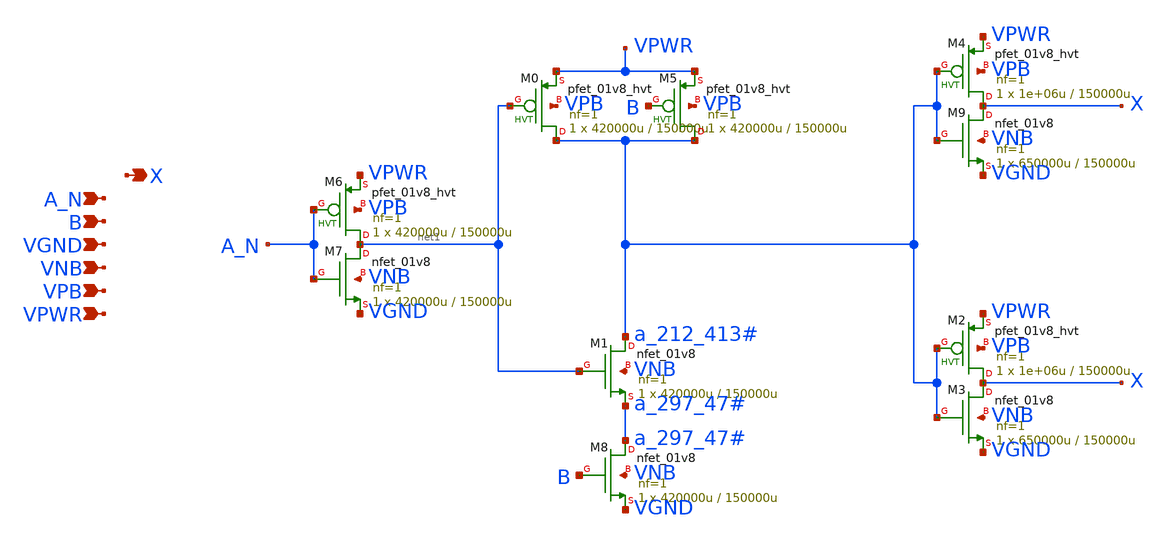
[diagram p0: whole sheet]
** sch_path: schematics/and2b/sky130_fd_sc_hd__and2b_2.sch
**.subckt sky130_fd_sc_hd__and2b_2 A_N B VGND VNB VPB VPWR X
*.ipin A_N
*.ipin B
*.ipin VGND
*.ipin VNB
*.ipin VPB
*.ipin VPWR
*.opin X
XM2 X a_212_413# VPWR VPB sky130_fd_pr__pfet_01v8_hvt L=150000u W=1e+06u nf=1 ad='int((1 + 1)/2) * 1e+06u / 1 * 0.29'
+ as='int((1 + 2)/2) * 1e+06u / 1 * 0.29' pd='2*int((1 + 1)/2) * (1e+06u / 1 + 0.29)' ps='2*int((1 + 2)/2) * (1e+06u / 1 + 0.29)'
+ nrd='0.29 / 1e+06u ' nrs='0.29 / 1e+06u ' sa=0 sb=0 sd=0 mult=1 m=1
XM3 X a_212_413# VGND VNB sky130_fd_pr__nfet_01v8 L=150000u W=650000u nf=1 ad='int((1 + 1)/2) * 650000u / 1 * 0.29'
+ as='int((1 + 2)/2) * 650000u / 1 * 0.29' pd='2*int((1 + 1)/2) * (650000u / 1 + 0.29)' ps='2*int((1 + 2)/2) * (650000u / 1 + 0.29)'
+ nrd='0.29 / 650000u ' nrs='0.29 / 650000u ' sa=0 sb=0 sd=0 mult=1 m=1
XM4 X a_212_413# VPWR VPB sky130_fd_pr__pfet_01v8_hvt L=150000u W=1e+06u nf=1 ad='int((1 + 1)/2) * 1e+06u / 1 * 0.29'
+ as='int((1 + 2)/2) * 1e+06u / 1 * 0.29' pd='2*int((1 + 1)/2) * (1e+06u / 1 + 0.29)' ps='2*int((1 + 2)/2) * (1e+06u / 1 + 0.29)'
+ nrd='0.29 / 1e+06u ' nrs='0.29 / 1e+06u ' sa=0 sb=0 sd=0 mult=1 m=1
XM9 X a_212_413# VGND VNB sky130_fd_pr__nfet_01v8 L=150000u W=650000u nf=1 ad='int((1 + 1)/2) * 650000u / 1 * 0.29'
+ as='int((1 + 2)/2) * 650000u / 1 * 0.29' pd='2*int((1 + 1)/2) * (650000u / 1 + 0.29)' ps='2*int((1 + 2)/2) * (650000u / 1 + 0.29)'
+ nrd='0.29 / 650000u ' nrs='0.29 / 650000u ' sa=0 sb=0 sd=0 mult=1 m=1
XM6 net1 A_N VPWR VPB sky130_fd_pr__pfet_01v8_hvt L=150000u W=420000u nf=1 ad='int((1 + 1)/2) * 420000u / 1 * 0.29'
+ as='int((1 + 2)/2) * 420000u / 1 * 0.29' pd='2*int((1 + 1)/2) * (420000u / 1 + 0.29)' ps='2*int((1 + 2)/2) * (420000u / 1 + 0.29)'
+ nrd='0.29 / 420000u ' nrs='0.29 / 420000u ' sa=0 sb=0 sd=0 mult=1 m=1
XM7 net1 A_N VGND VNB sky130_fd_pr__nfet_01v8 L=150000u W=420000u nf=1 ad='int((1 + 1)/2) * 420000u / 1 * 0.29'
+ as='int((1 + 2)/2) * 420000u / 1 * 0.29' pd='2*int((1 + 1)/2) * (420000u / 1 + 0.29)' ps='2*int((1 + 2)/2) * (420000u / 1 + 0.29)'
+ nrd='0.29 / 420000u ' nrs='0.29 / 420000u ' sa=0 sb=0 sd=0 mult=1 m=1
XM0 a_212_413# net1 VPWR VPB sky130_fd_pr__pfet_01v8_hvt L=150000u W=420000u nf=1 ad='int((1 + 1)/2) * 420000u / 1 * 0.29'
+ as='int((1 + 2)/2) * 420000u / 1 * 0.29' pd='2*int((1 + 1)/2) * (420000u / 1 + 0.29)' ps='2*int((1 + 2)/2) * (420000u / 1 + 0.29)'
+ nrd='0.29 / 420000u ' nrs='0.29 / 420000u ' sa=0 sb=0 sd=0 mult=1 m=1
XM5 a_212_413# B VPWR VPB sky130_fd_pr__pfet_01v8_hvt L=150000u W=420000u nf=1 ad='int((1 + 1)/2) * 420000u / 1 * 0.29'
+ as='int((1 + 2)/2) * 420000u / 1 * 0.29' pd='2*int((1 + 1)/2) * (420000u / 1 + 0.29)' ps='2*int((1 + 2)/2) * (420000u / 1 + 0.29)'
+ nrd='0.29 / 420000u ' nrs='0.29 / 420000u ' sa=0 sb=0 sd=0 mult=1 m=1
XM1 a_212_413# net1 a_297_47# VNB sky130_fd_pr__nfet_01v8 L=150000u W=420000u nf=1 ad='int((1 + 1)/2) * 420000u / 1 * 0.29'
+ as='int((1 + 2)/2) * 420000u / 1 * 0.29' pd='2*int((1 + 1)/2) * (420000u / 1 + 0.29)' ps='2*int((1 + 2)/2) * (420000u / 1 + 0.29)'
+ nrd='0.29 / 420000u ' nrs='0.29 / 420000u ' sa=0 sb=0 sd=0 mult=1 m=1
XM8 a_297_47# B VGND VNB sky130_fd_pr__nfet_01v8 L=150000u W=420000u nf=1 ad='int((1 + 1)/2) * 420000u / 1 * 0.29'
+ as='int((1 + 2)/2) * 420000u / 1 * 0.29' pd='2*int((1 + 1)/2) * (420000u / 1 + 0.29)' ps='2*int((1 + 2)/2) * (420000u / 1 + 0.29)'
+ nrd='0.29 / 420000u ' nrs='0.29 / 420000u ' sa=0 sb=0 sd=0 mult=1 m=1
**.ends
.end
